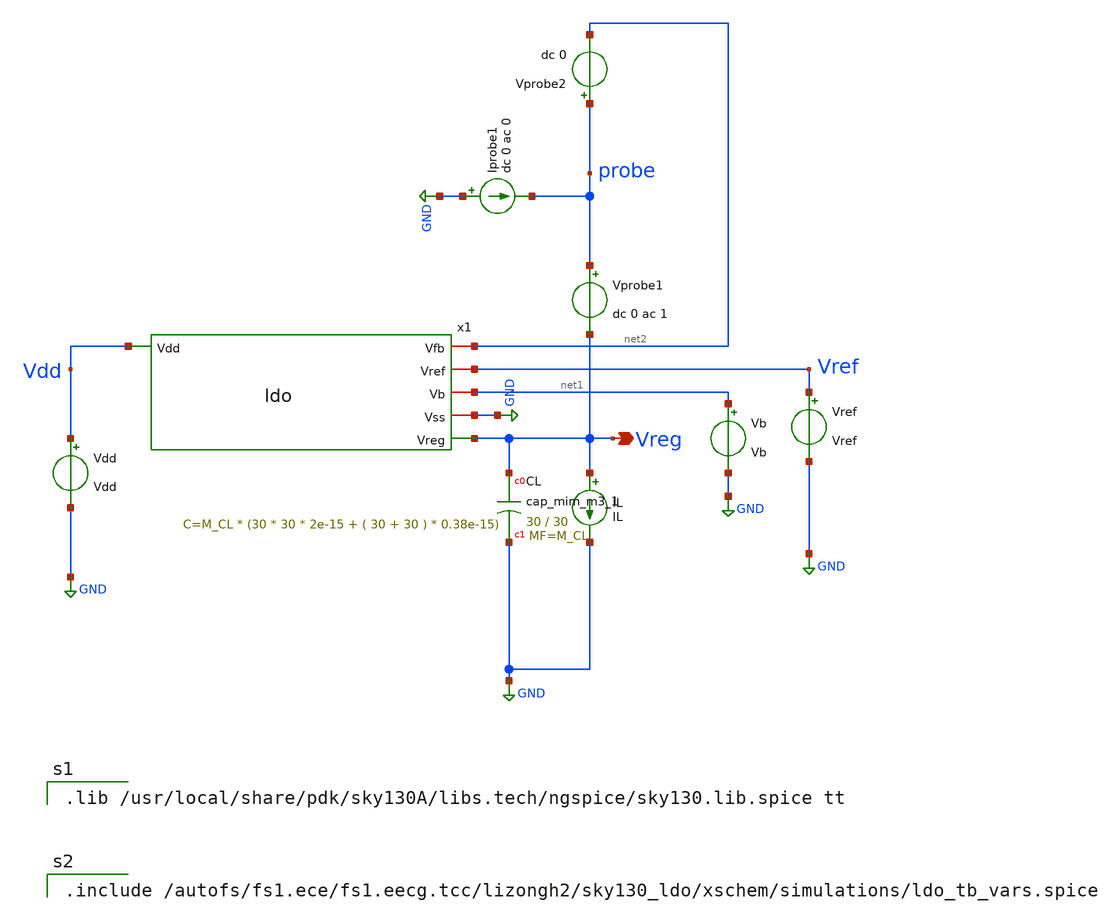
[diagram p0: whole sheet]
** sch_path: xschem/ldo_tb_stb_middlebrook.sch
**.subckt ldo_tb_stb_middlebrook Vreg
*.opin Vreg
Vref Vref GND Vref
Vb net1 GND Vb
IL Vreg GND IL
Vdd Vdd GND Vdd
x1 Vdd net2 Vref net1 GND Vreg ldo
XCL Vreg GND sky130_fd_pr__cap_mim_m3_1 W=30 L=30 MF=M_CL m=M_CL
Vprobe2 probe net2 dc 0
Vprobe1 probe Vreg dc 0 ac 1
Iprobe1 GND probe dc 0 ac 0
**** begin user architecture code

.lib /usr/local/share/pdk/sky130A/libs.tech/ngspice/sky130.lib.spice tt




.nodeset v(Vreg)=1.8
.nodeset v(net2)=1.8

.control
save all
set filetype=ascii
set units=degrees

* Stability_Analysis using Middlebrook and Tian's method
* http://education.ingenazure.com/ac-stability-analysis-ngspice/
* at min load
alter IL dc=10u
let runs=2
let run=0

alter @Vprobe1[acmag]=1
alter @Iprobe1[acmag]=0

dowhile run<runs
set run=$&run
set temp=27

ac dec 10 1 10G

alter @Vprobe1[acmag]=0
alter @Iprobe1[acmag]=1

let run=run+1
end

let ip11 = ac1.i(Vprobe1)
let ip12 = ac1.i(Vprobe2)
let ip21 = ac2.i(Vprobe1)
let ip22 = ac2.i(Vprobe2)
let vprb1 = ac1.v(probe)
let vprb2 = ac2.v(probe)

*** Middlebrook
let mb = 1/(vprb1+ip22)-1
*** Tian that is preferred
let av = 1/(1/(2*(ip11*vprb2-vprb1*ip21)+vprb1+ip21)-1)

plot vdb(mb) vp(mb)
plot vdb(av) vp(av)

wrdata ldo_tb_loop_gain_minload mag(av) vp(av)

* at max load
reset all
alter IL dc=10m
let runs=2
let run=0

alter @Vprobe1[acmag]=1
alter @Iprobe1[acmag]=0

dowhile run<runs
set run=$&run
set temp=27

ac dec 10 1 10G

alter @Vprobe1[acmag]=0
alter @Iprobe1[acmag]=1

let run=run+1
end

let ip11 = ac3.i(Vprobe1)
let ip12 = ac3.i(Vprobe2)
let ip21 = ac4.i(Vprobe1)
let ip22 = ac4.i(Vprobe2)
let vprb1 = ac3.v(probe)
let vprb2 = ac4.v(probe)

*** Middlebrook
let mb = 1/(vprb1+ip22)-1
*** Tian that is preferred
let av = 1/(1/(2*(ip11*vprb2-vprb1*ip21)+vprb1+ip21)-1)

plot vdb(mb) vp(mb)
plot vdb(av) vp(av)

wrdata ldo_tb_loop_gain_maxload mag(av) vp(av)

.endc



.include /autofs/fs1.ece/fs1.eecg.tcc/lizongh2/sky130_ldo/xschem/simulations/ldo_tb_vars.spice


**** end user architecture code
**.ends

* expanding   symbol:  ldo.sym # of pins=6
** sym_path: xschem/ldo.sym
** sch_path: xschem/ldo.sch
.subckt ldo Vdd Vfb Vref Vb Vss Vreg
*.iopin Vb
*.iopin Vss
*.opin Vreg
*.iopin Vref
*.ipin Vdd
*.iopin Vfb
x1 Vdd net1 Vfb Vref Vb Vss diff_pair
XM6 Vreg net1 Vdd Vdd sky130_fd_pr__pfet_g5v0d10v5 L=L_pass W=W_pass nf=Nf_pass ad='int((nf+1)/2) * W/nf
+ * 0.29' as='int((nf+2)/2) * W/nf * 0.29' pd='2*int((nf+1)/2) * (W/nf + 0.29)' ps='2*int((nf+2)/2) * (W/nf
+ + 0.29)' nrd='0.29 / W' nrs='0.29 / W' sa=0 sb=0 sd=0 mult=M_pass m=M_pass
XCfb net2 Vreg sky130_fd_pr__cap_mim_m3_1 W=10 L=10 MF=M_Cfb m=M_Cfb
XRfb net2 net1 Vss sky130_fd_pr__res_high_po_0p35 L=3 mult=M_Rfb m=M_Rfb
.ends


* expanding   symbol:  diff_pair.sym # of pins=6
** sym_path: xschem/diff_pair.sym
** sch_path: xschem/diff_pair.sch
.subckt diff_pair Vdd vout vinp vinm Vb Vss
*.iopin Vdd
*.ipin vinm
*.ipin vinp
*.iopin Vb
*.opin vout
*.iopin Vss
XM1 net1 vinp net2 Vss sky130_fd_pr__nfet_g5v0d10v5 L=L_M1 W=W_M1 nf=1 ad='int((nf+1)/2) * W/nf * 0.29' as='int((nf+2)/2)
+ * W/nf * 0.29' pd='2*int((nf+1)/2) * (W/nf + 0.29)' ps='2*int((nf+2)/2) * (W/nf + 0.29)' nrd='0.29 /
+ W' nrs='0.29 / W' sa=0 sb=0 sd=0 mult=1 m=1
XM2 vout vinm net2 Vss sky130_fd_pr__nfet_g5v0d10v5 L=L_M2 W=W_M2 nf=1 ad='int((nf+1)/2) * W/nf * 0.29' as='int((nf+2)/2)
+ * W/nf * 0.29' pd='2*int((nf+1)/2) * (W/nf + 0.29)' ps='2*int((nf+2)/2) * (W/nf + 0.29)' nrd='0.29 /
+ W' nrs='0.29 / W' sa=0 sb=0 sd=0 mult=1 m=1
XM3 vout net1 Vdd Vdd sky130_fd_pr__pfet_g5v0d10v5 L=L_M3 W=W_M3 nf=1 ad='int((nf+1)/2) * W/nf * 0.29' as='int((nf+2)/2)
+ * W/nf * 0.29' pd='2*int((nf+1)/2) * (W/nf + 0.29)' ps='2*int((nf+2)/2) * (W/nf + 0.29)' nrd='0.29 /
+ W' nrs='0.29 / W' sa=0 sb=0 sd=0 mult=1 m=1
XM4 net1 net1 Vdd Vdd sky130_fd_pr__pfet_g5v0d10v5 L=L_M4 W=W_M4 nf=1 ad='int((nf+1)/2) * W/nf * 0.29' as='int((nf+2)/2)
+ * W/nf * 0.29' pd='2*int((nf+1)/2) * (W/nf + 0.29)' ps='2*int((nf+2)/2) * (W/nf + 0.29)' nrd='0.29 /
+ W' nrs='0.29 / W' sa=0 sb=0 sd=0 mult=1 m=1
XM5 net2 Vb Vss Vss sky130_fd_pr__nfet_g5v0d10v5 L=L_M5 W=W_M5 nf=1 ad='int((nf+1)/2) * W/nf * 0.29' as='int((nf+2)/2)
+ * W/nf * 0.29' pd='2*int((nf+1)/2) * (W/nf + 0.29)' ps='2*int((nf+2)/2) * (W/nf + 0.29)' nrd='0.29 /
+ W' nrs='0.29 / W' sa=0 sb=0 sd=0 mult=1 m=1
.ends

.GLOBAL GND
.end
